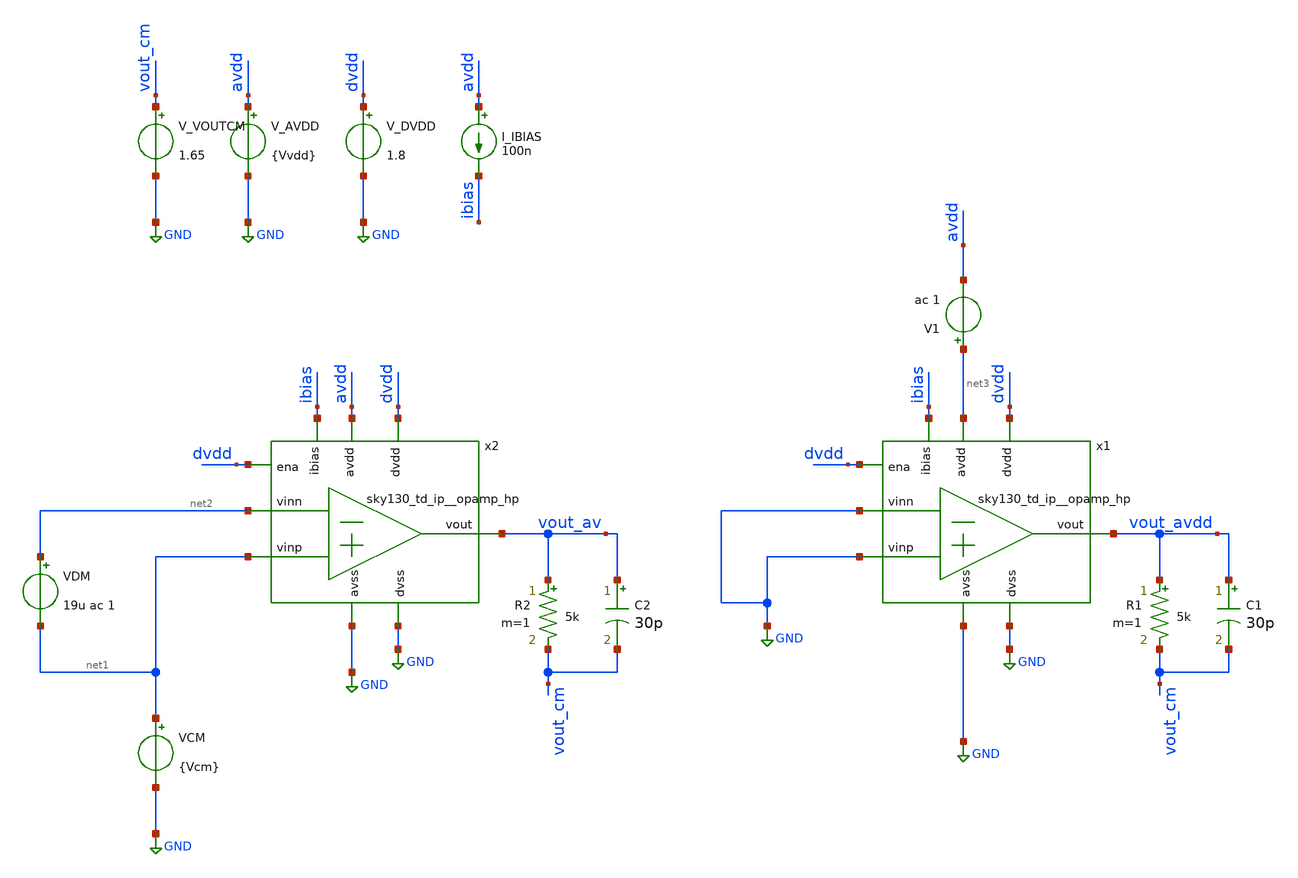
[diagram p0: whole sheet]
** sch_path: cace/psrrp.sch
**.subckt psrrp
x1 net3 vout_avdd ibias GND GND GND dvdd GND dvdd sky130_td_ip__opamp_hp
V_AVDD avdd GND {Vvdd}
.save i(v_avdd)
V_DVDD dvdd GND 1.8
.save i(v_dvdd)
I_IBIAS avdd ibias 100n
R1 vout_avdd vout_cm 5k m=1
C1 vout_avdd vout_cm 30p m=1
V_VOUTCM vout_cm GND 1.65
.save i(v_voutcm)
V1 net3 avdd ac 1
x2 avdd vout_av ibias net2 net1 GND dvdd GND dvdd sky130_td_ip__opamp_hp
R2 vout_av vout_cm 5k m=1
C2 vout_av vout_cm 30p m=1
VDM net2 net1 19u ac 1
VCM net1 GND {Vcm}
.save i(vcm)
**** begin user architecture code


.control
save all

* Calculate input offset voltage
dc VDM -1m 1m 100u
run
let vout = v(vout)
meas DC input_offset_voltage WHEN vout=1.65
let offset = $&input_offset_voltage
alter VDM dc = $&input_offset_voltage
alter VDM ac = 1

* Run AC sweep from 1Hz to 1GHz
AC DEC 100 1 1000000000
run

* Get DC gain in DBs.
let av_db = db(vout_av)
let avdd_db = db(vout_avdd)
let psrrp_db = av_db - avdd_db

meas AC psrrp_dc FIND psrrp_db AT=1
meas AC psrrp_10k FIND psrrp_db AT=10K

echo
echo ===================================
echo PSRR+ characterization results:
echo - PSRR @ 1 Hz: $&psrrp_dc
echo - PSRR @ 10 kHz: $&psrrp_10k
echo ===================================

echo $&psrrp_dc $&psrrp_10k > {simpath}/{filename}_{N}.data
quit
.endc




* CACE gensim simulation file {filename}_{N}
* Generated by CACE gensim, Efabless Corporation (c) 2023
* Find the power supply rejection ratio of the amplifier

.include {DUT_path}

.lib {PDK_ROOT}/{PDK}/libs.tech/combined/sky130.lib.spice {corner}

.option TEMP={temperature}
* Flag unsafe operating conditions (exceeds models' specified limits)
.option warn=1
.option SEED=[{seed=12345} + {iterations=0}]


**** end user architecture code
**.ends
.GLOBAL GND
.end
